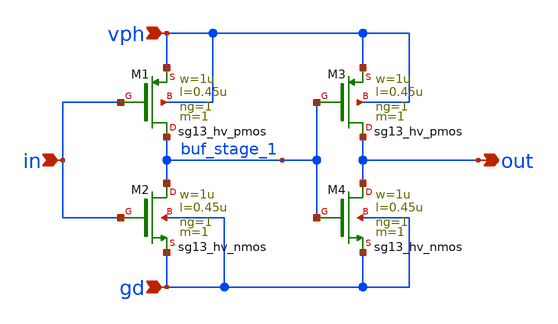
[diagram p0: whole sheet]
** sch_path: schematics/misc/buffer_hv.sch
**.subckt buffer_hv in out vph gd
*.ipin in
*.opin out
*.ipin vph
*.ipin gd
XM1 buf_stage_1 in vph vph sg13_hv_pmos w=1u l=0.45u ng=1 m=1 mm_ok=1
XM2 buf_stage_1 in gd gd sg13_hv_nmos w=1u l=0.45u ng=1 m=1 mm_ok=1
XM3 out buf_stage_1 vph vph sg13_hv_pmos w=1u l=0.45u ng=1 m=1 mm_ok=1
XM4 out buf_stage_1 gd gd sg13_hv_nmos w=1u l=0.45u ng=1 m=1 mm_ok=1
**.ends
.end
